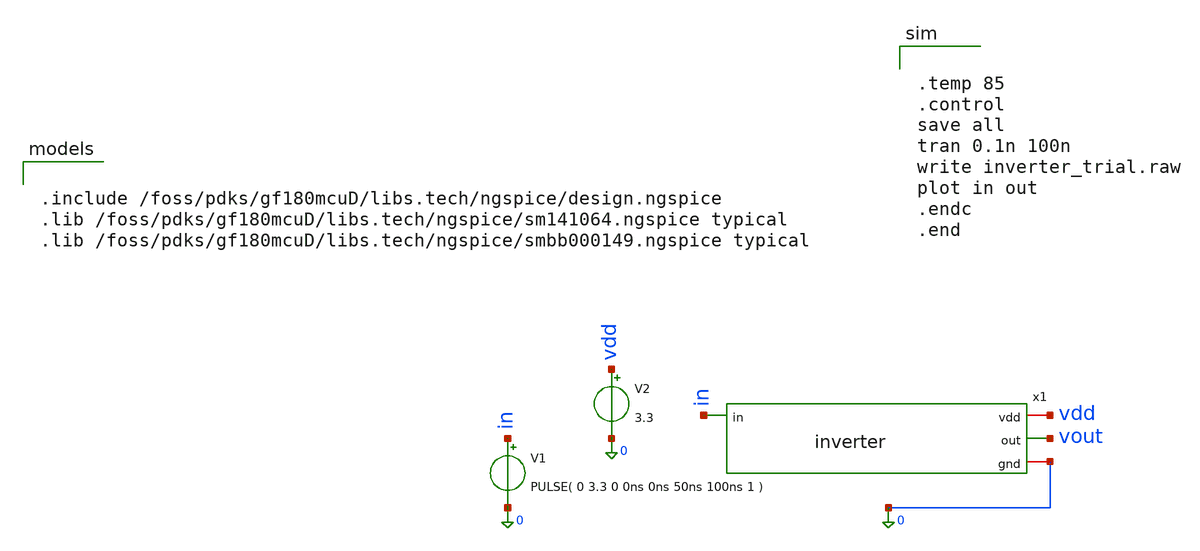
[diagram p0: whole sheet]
** sch_path: xschem/c2v_frontend/inverter_test.sch
**.subckt inverter_test
x1 vdd in vout 0 inverter
V1 in 0 PULSE( 0 3.3 0 0ns 0ns 50ns 100ns 1 )
V2 vdd 0 3.3
**** begin user architecture code


.temp 85
.control
save all
tran 0.1n 100n
write inverter_trial.raw
plot in out
.endc
.end




.include /foss/pdks/gf180mcuD/libs.tech/ngspice/design.ngspice
.lib /foss/pdks/gf180mcuD/libs.tech/ngspice/sm141064.ngspice typical
.lib /foss/pdks/gf180mcuD/libs.tech/ngspice/smbb000149.ngspice typical


**** end user architecture code
**.ends

* expanding   symbol:  inverter.sym # of pins=4
** sym_path: xschem/c2v_frontend/inverter.sym
** sch_path: xschem/c2v_frontend/inverter.sch
.subckt inverter vdd in out gnd
*.iopin vdd
*.iopin gnd
*.ipin in
*.opin out
XM1 out in vdd vdd pfet_03v3 L=1u W=5u nf=1 ad='int((nf+1)/2) * W/nf * 0.18u' as='int((nf+2)/2) * W/nf * 0.18u'
+ pd='2*int((nf+1)/2) * (W/nf + 0.18u)' ps='2*int((nf+2)/2) * (W/nf + 0.18u)' nrd='0.18u / W' nrs='0.18u / W'
+ sa=0 sb=0 sd=0 m=1
XM2 out in gnd gnd nfet_03v3 L=0.28u W=0.22u nf=1 ad='int((nf+1)/2) * W/nf * 0.18u' as='int((nf+2)/2) * W/nf * 0.18u'
+ pd='2*int((nf+1)/2) * (W/nf + 0.18u)' ps='2*int((nf+2)/2) * (W/nf + 0.18u)' nrd='0.18u / W' nrs='0.18u / W'
+ sa=0 sb=0 sd=0 m=1
.ends

.end
